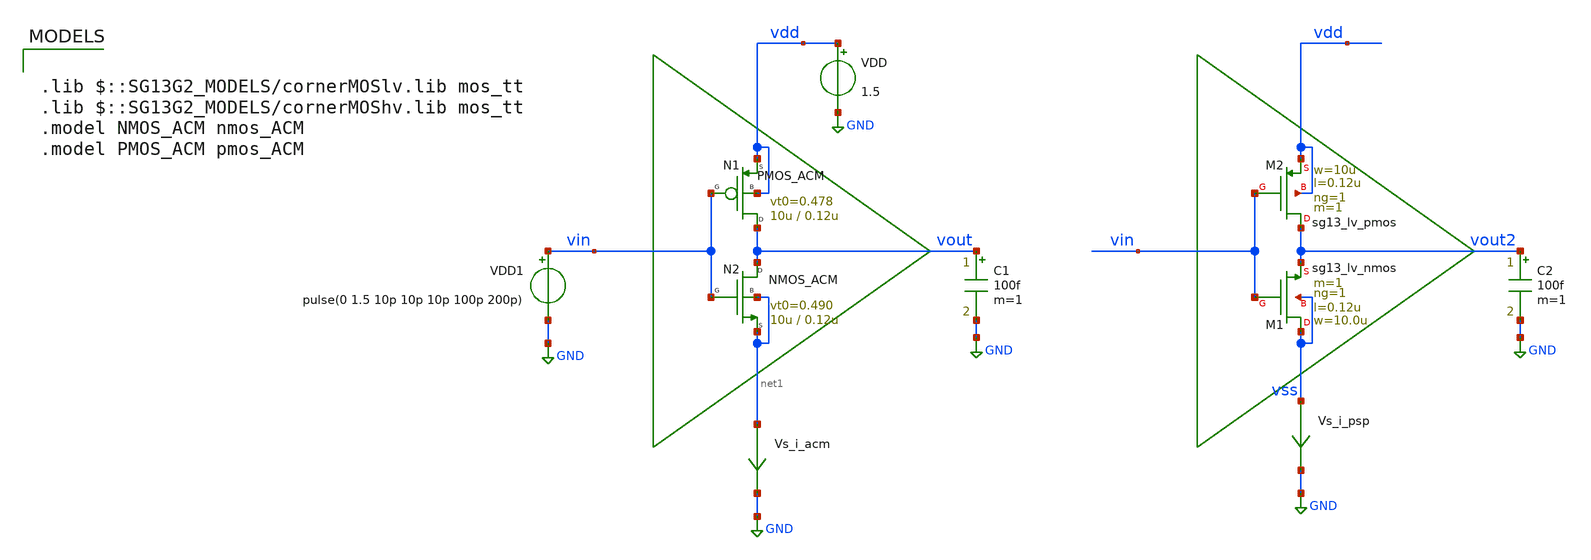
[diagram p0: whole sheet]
** sch_path: legacy/Examples/IHP-SG13/xschem/TB_inv_acm_step.sch
**.subckt TB_inv_acm_step
VDD vdd GND 1.5
N2 vout vin net1 net1 NMOS_ACM w=10u l=0.12u n=1.41 is=11.78u vt0=0.490 sigma=53mm zeta=7m
N1 vout vin vdd vdd PMOS_ACM w=10u l=0.12u n=1.46 is=9.39u vt0=0.478 sigma=48m zeta=31m
Vs_i_psp vss GND 0
.save i(vs_i_psp)
Vs_i_acm net1 GND 0
.save i(vs_i_acm)
XM1 vss vin vout2 vss sg13_lv_nmos w=10.0u l=0.12u ng=1 m=1 mm_ok=1
XM2 vout2 vin vdd vdd sg13_lv_pmos w=10u l=0.12u ng=1 m=1 mm_ok=1
VDD1 vin GND pulse(0 1.5 10p 10p 10p 100p 200p)
C1 vout GND 100f m=1
C2 vout2 GND 100f m=1
**** begin user architecture code


.control
pre_osdi ./NMOS_ACM_2V0.osdi
pre_osdi ./PMOS_ACM_2V0.osdi
pre_osdi ./psp103_nqs.osdi
save all

tran 0.1p 80p
remzerovec
write TB_inv_acm_step.raw
set appendwrite

.endc



.lib $::SG13G2_MODELS/cornerMOSlv.lib mos_tt
.lib $::SG13G2_MODELS/cornerMOShv.lib mos_tt
.model NMOS_ACM nmos_ACM
.model PMOS_ACM pmos_ACM

**** end user architecture code
**.ends
.GLOBAL GND
.end
